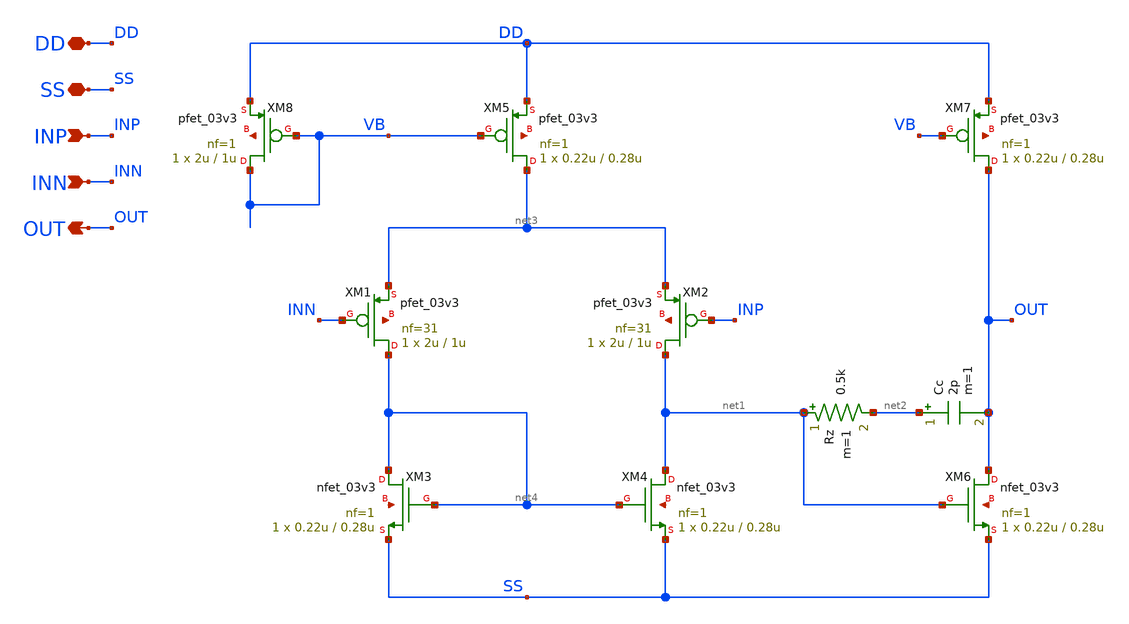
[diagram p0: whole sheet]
** sch_path: Design_Files/IC Design/Schematic/Single_ended_OTA/Single_ended_OTA.sch
**.subckt Single_ended_OTA DD SS INP INN OUT
*.iopin DD
*.iopin SS
*.ipin INP
*.ipin INN
*.opin OUT
XM4 net1 net4 SS net5 nfet_03v3 L=0.28u W=0.22u nf=1 ad='int((nf+1)/2) * W/nf * 0.18u' as='int((nf+2)/2) * W/nf * 0.18u'
+ pd='2*int((nf+1)/2) * (W/nf + 0.18u)' ps='2*int((nf+2)/2) * (W/nf + 0.18u)' nrd='0.18u / W' nrs='0.18u / W'
+ sa=0 sb=0 sd=0 m=1
XM3 net4 net4 SS net6 nfet_03v3 L=0.28u W=0.22u nf=1 ad='int((nf+1)/2) * W/nf * 0.18u' as='int((nf+2)/2) * W/nf * 0.18u'
+ pd='2*int((nf+1)/2) * (W/nf + 0.18u)' ps='2*int((nf+2)/2) * (W/nf + 0.18u)' nrd='0.18u / W' nrs='0.18u / W'
+ sa=0 sb=0 sd=0 m=1
XM1 net4 INN net3 net7 pfet_03v3 L=1u W=2u nf=31 ad='int((nf+1)/2) * W/nf * 0.18u' as='int((nf+2)/2) * W/nf * 0.18u'
+ pd='2*int((nf+1)/2) * (W/nf + 0.18u)' ps='2*int((nf+2)/2) * (W/nf + 0.18u)' nrd='0.18u / W' nrs='0.18u / W'
+ sa=0 sb=0 sd=0 m=1
XM2 net1 INP net3 net8 pfet_03v3 L=1u W=2u nf=31 ad='int((nf+1)/2) * W/nf * 0.18u' as='int((nf+2)/2) * W/nf * 0.18u'
+ pd='2*int((nf+1)/2) * (W/nf + 0.18u)' ps='2*int((nf+2)/2) * (W/nf + 0.18u)' nrd='0.18u / W' nrs='0.18u / W'
+ sa=0 sb=0 sd=0 m=1
XM7 OUT VB DD net9 pfet_03v3 L=0.28u W=0.22u nf=1 ad='int((nf+1)/2) * W/nf * 0.18u' as='int((nf+2)/2) * W/nf * 0.18u'
+ pd='2*int((nf+1)/2) * (W/nf + 0.18u)' ps='2*int((nf+2)/2) * (W/nf + 0.18u)' nrd='0.18u / W' nrs='0.18u / W'
+ sa=0 sb=0 sd=0 m=1
Rz net1 net2 0.5k m=1
XM5 net3 VB DD net10 pfet_03v3 L=0.28u W=0.22u nf=1 ad='int((nf+1)/2) * W/nf * 0.18u' as='int((nf+2)/2) * W/nf * 0.18u'
+ pd='2*int((nf+1)/2) * (W/nf + 0.18u)' ps='2*int((nf+2)/2) * (W/nf + 0.18u)' nrd='0.18u / W' nrs='0.18u / W'
+ sa=0 sb=0 sd=0 m=1
XM6 OUT net1 SS net11 nfet_03v3 L=0.28u W=0.22u nf=1 ad='int((nf+1)/2) * W/nf * 0.18u' as='int((nf+2)/2) * W/nf * 0.18u'
+ pd='2*int((nf+1)/2) * (W/nf + 0.18u)' ps='2*int((nf+2)/2) * (W/nf + 0.18u)' nrd='0.18u / W' nrs='0.18u / W'
+ sa=0 sb=0 sd=0 m=1
XM8 VB VB DD net12 pfet_03v3 L=1u W=2u nf=1 ad='int((nf+1)/2) * W/nf * 0.18u' as='int((nf+2)/2) * W/nf * 0.18u'
+ pd='2*int((nf+1)/2) * (W/nf + 0.18u)' ps='2*int((nf+2)/2) * (W/nf + 0.18u)' nrd='0.18u / W' nrs='0.18u / W'
+ sa=0 sb=0 sd=0 m=1
Cc net2 OUT 2p m=1
**.ends
.end
